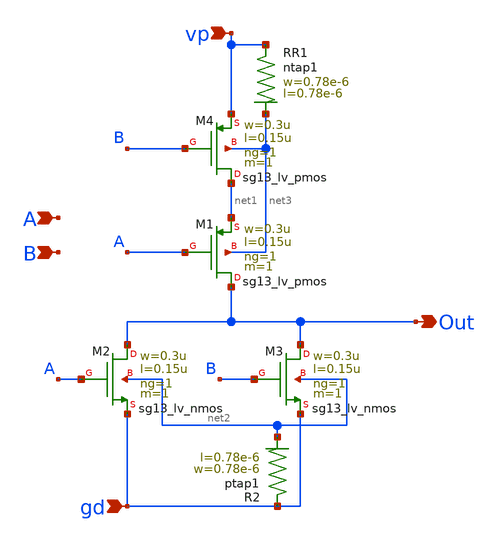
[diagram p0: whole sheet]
** sch_path: schematics/PFD/PFD_NOR.sch
**.subckt PFD_NOR vp gd B A Out
*.ipin vp
*.ipin gd
*.ipin B
*.ipin A
*.opin Out
XM1 Out A net1 net3 sg13_lv_pmos w=0.3u l=0.15u ng=1 m=1 mm_ok=1
XM4 net1 B vp net3 sg13_lv_pmos w=0.3u l=0.15u ng=1 m=1 mm_ok=1
XM2 Out A gd net2 sg13_lv_nmos w=0.3u l=0.15u ng=1 m=1 mm_ok=1
XM3 Out B gd net2 sg13_lv_nmos w=0.3u l=0.15u ng=1 m=1 mm_ok=1
XR1 vp net3 ntap1 R=262.8 w=0.78e-6 l=0.78e-6
XR2 gd net2 ptap1 R=262.8 w=0.78e-6 l=0.78e-6
**.ends
.end
